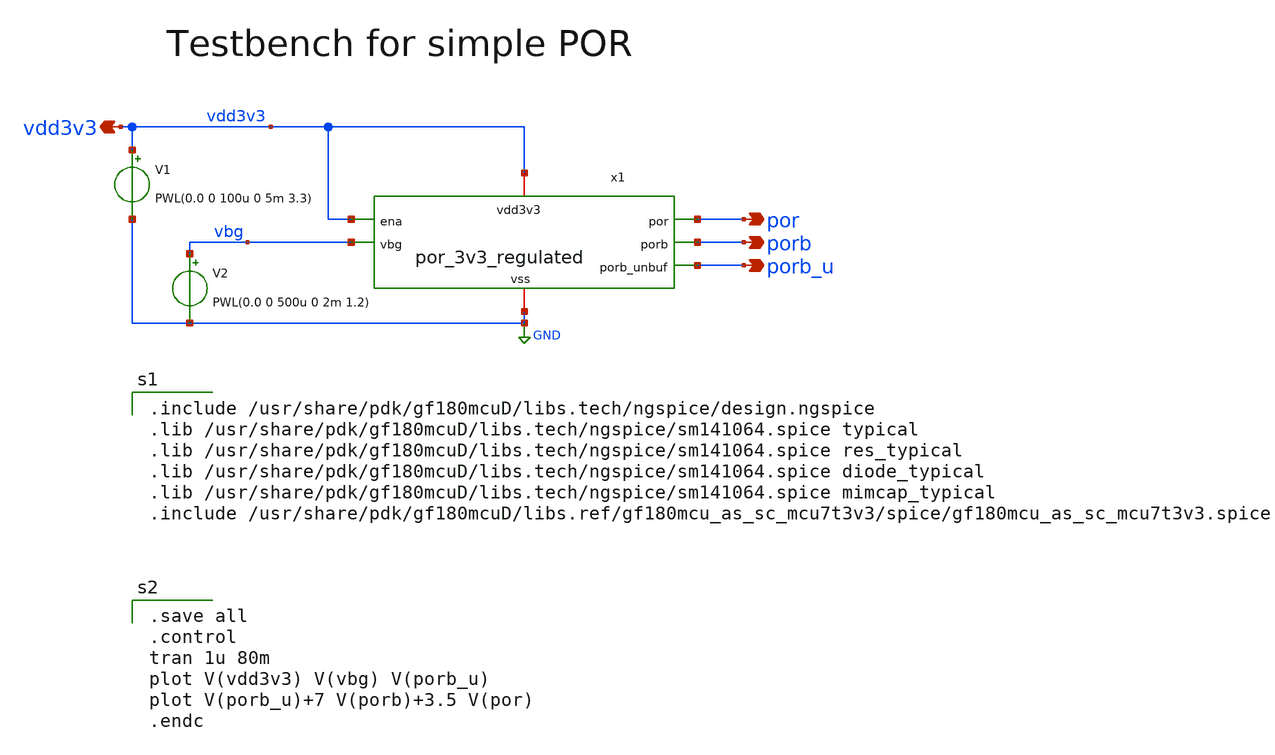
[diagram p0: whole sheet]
** sch_path: projects/programmable_transceiver_platform/analog/core_support/por/xschem/simple_por_tb.sch
**.subckt simple_por_tb vdd3v3 porb_u porb por
*.opin vdd3v3
*.opin porb_u
*.opin porb
*.opin por
V1 vdd3v3 GND PWL(0.0 0 100u 0 5m 3.3)
x1 vdd3v3 vbg vdd3v3 porb_u GND porb por por_3v3_regulated
V2 vbg GND PWL(0.0 0 500u 0 2m 1.2)
**** begin user architecture code

.save all
.control
tran 1u 80m
plot V(vdd3v3) V(vbg) V(porb_u)
plot V(porb_u)+7 V(porb)+3.5 V(por)
.endc


.include /usr/share/pdk/gf180mcuD/libs.tech/ngspice/design.ngspice
.lib /usr/share/pdk/gf180mcuD/libs.tech/ngspice/sm141064.spice typical
.lib /usr/share/pdk/gf180mcuD/libs.tech/ngspice/sm141064.spice res_typical
.lib /usr/share/pdk/gf180mcuD/libs.tech/ngspice/sm141064.spice diode_typical
.lib /usr/share/pdk/gf180mcuD/libs.tech/ngspice/sm141064.spice mimcap_typical
.include /usr/share/pdk/gf180mcuD/libs.ref/gf180mcu_as_sc_mcu7t3v3/spice/gf180mcu_as_sc_mcu7t3v3.spice

**** end user architecture code
**.ends
.GLOBAL GND
.end
